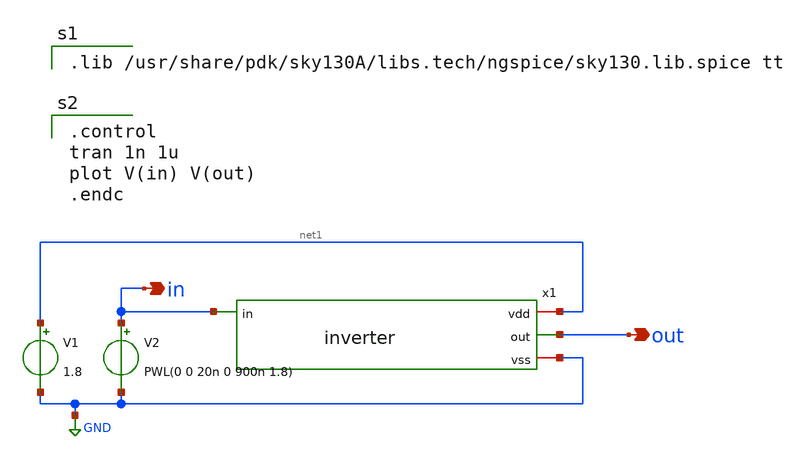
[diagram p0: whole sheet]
** sch_path: inverter/xschem/inverter_tb.sch
**.subckt inverter_tb in out
*.opin in
*.opin out
V1 net1 GND 1.8
V2 in GND PWL(0 0 20n 0 900n 1.8)
x1 net1 in out GND inverter
**** begin user architecture code

.lib /usr/share/pdk/sky130A/libs.tech/ngspice/sky130.lib.spice tt


.control
tran 1n 1u
plot V(in) V(out)
.endc

**** end user architecture code
**.ends

* expanding   symbol:  inverter.sym # of pins=4
** sym_path: day1/xschem/inverter.sym
** sch_path: day1/xschem/inverter.sch
.subckt inverter vdd in out vss
*.ipin in
*.opin out
*.iopin vss
*.iopin vdd
XM1 out in vss vss sky130_fd_pr__nfet_01v8 L=0.18 W=4.5 nf=3 ad='int((nf+1)/2) * W/nf * 0.29' as='int((nf+2)/2) * W/nf * 0.29'
+ pd='2*int((nf+1)/2) * (W/nf + 0.29)' ps='2*int((nf+2)/2) * (W/nf + 0.29)' nrd='0.29 / W' nrs='0.29 / W'
+ sa=0 sb=0 sd=0 mult=1 m=1
XM2 out in vdd vdd sky130_fd_pr__pfet_01v8 L=0.15 W=3 nf=3 ad='int((nf+1)/2) * W/nf * 0.29' as='int((nf+2)/2) * W/nf * 0.29'
+ pd='2*int((nf+1)/2) * (W/nf + 0.29)' ps='2*int((nf+2)/2) * (W/nf + 0.29)' nrd='0.29 / W' nrs='0.29 / W'
+ sa=0 sb=0 sd=0 mult=1 m=1
.ends

.GLOBAL GND
.end
